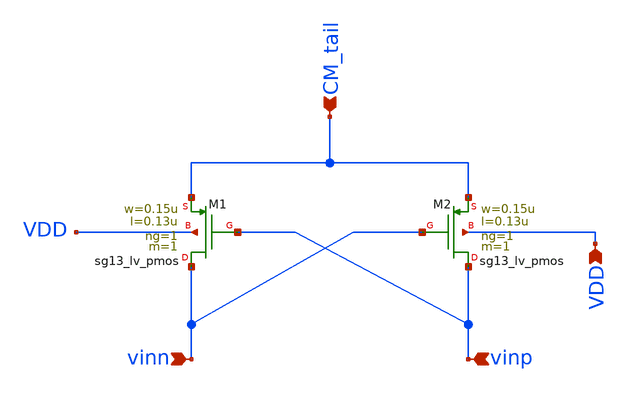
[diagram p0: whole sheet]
** sch_path: analog-db/templates/miscellaneous/cross_coupled_pmos.sch
* Copyright 2026 MacAnalog Research Group
**.subckt cross_coupled_pmos vinp vinn CM_tail VDD
*.ipin vinp
*.ipin vinn
*.ipin CM_tail
*.ipin VDD
XM1 vinn vinp CM_tail VDD sg13_lv_pmos w=0.15u l=0.13u ng=1 m=1 mm_ok=1
XM2 vinp vinn CM_tail VDD sg13_lv_pmos w=0.15u l=0.13u ng=1 m=1 mm_ok=1
**.ends
.end
